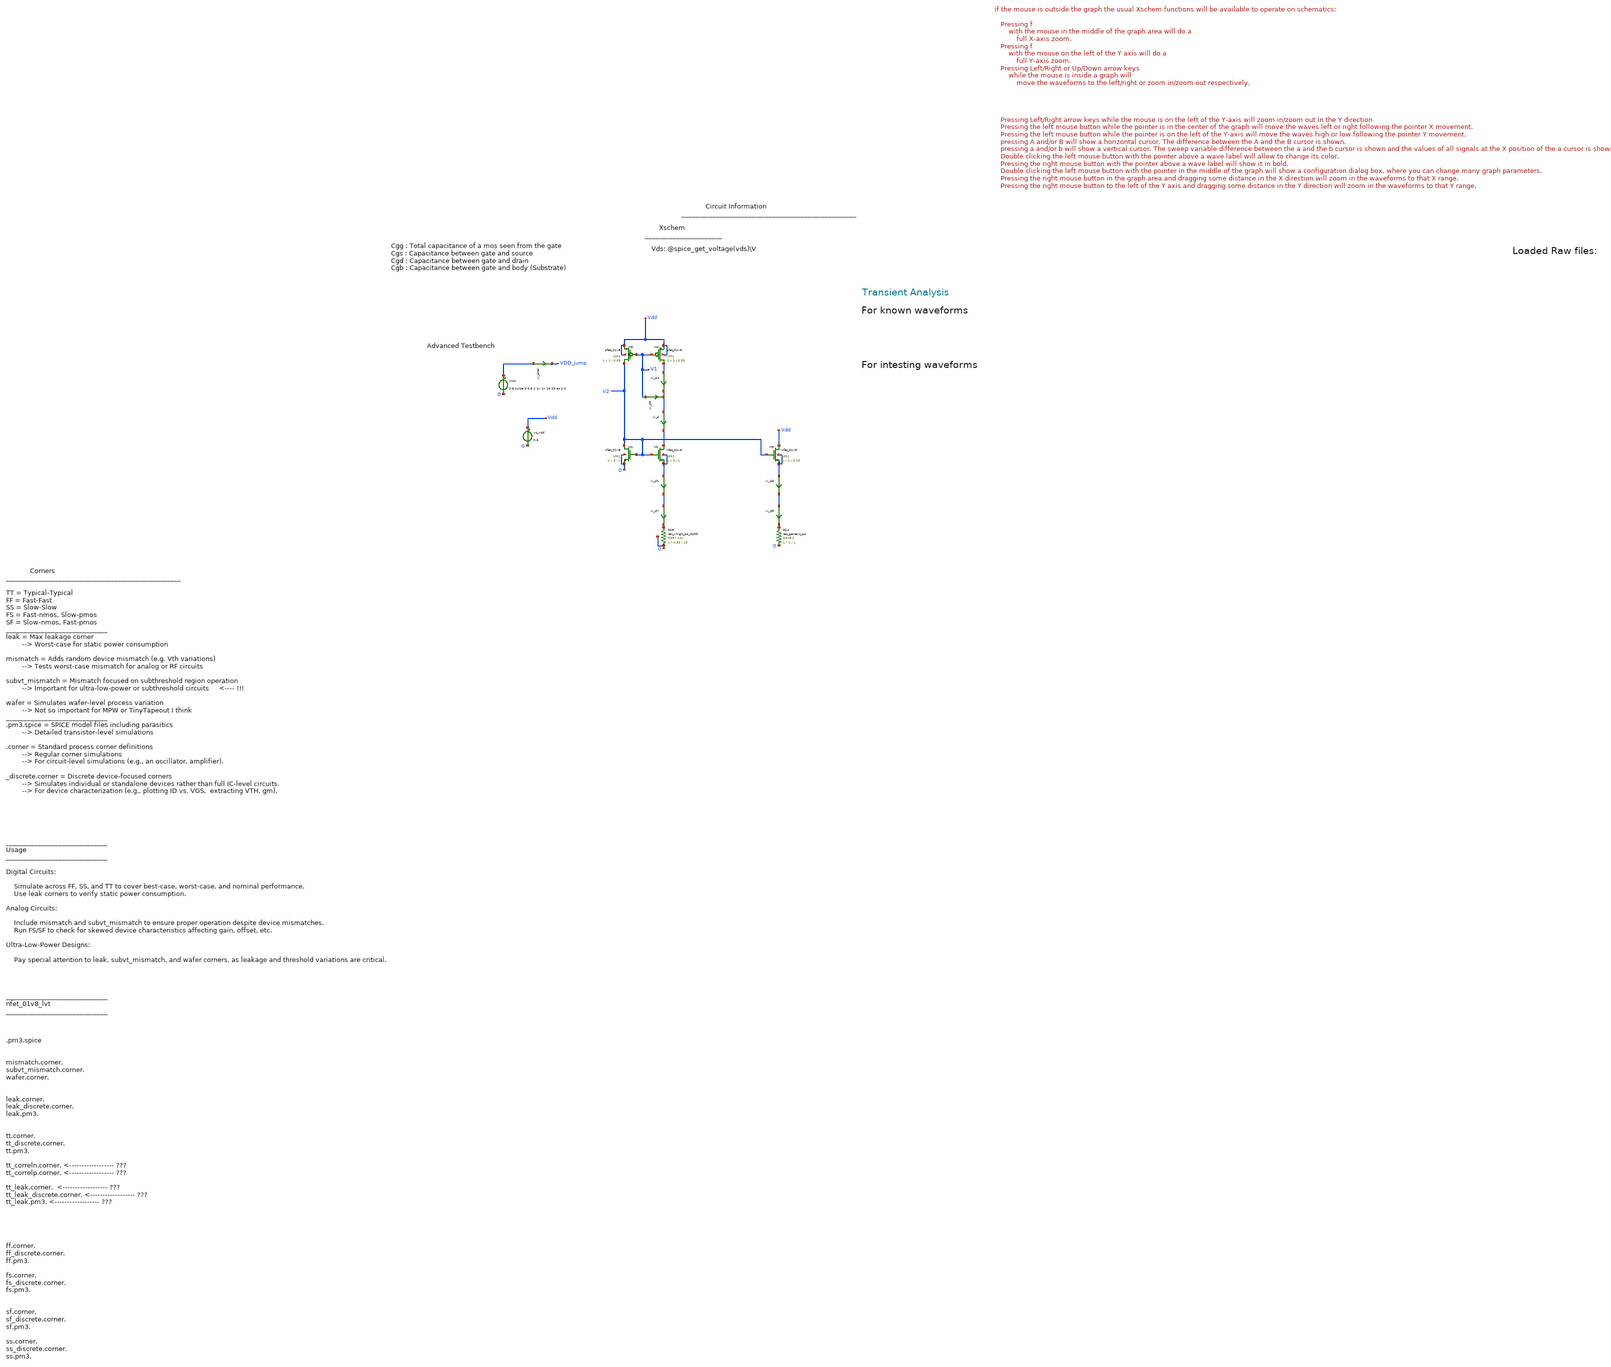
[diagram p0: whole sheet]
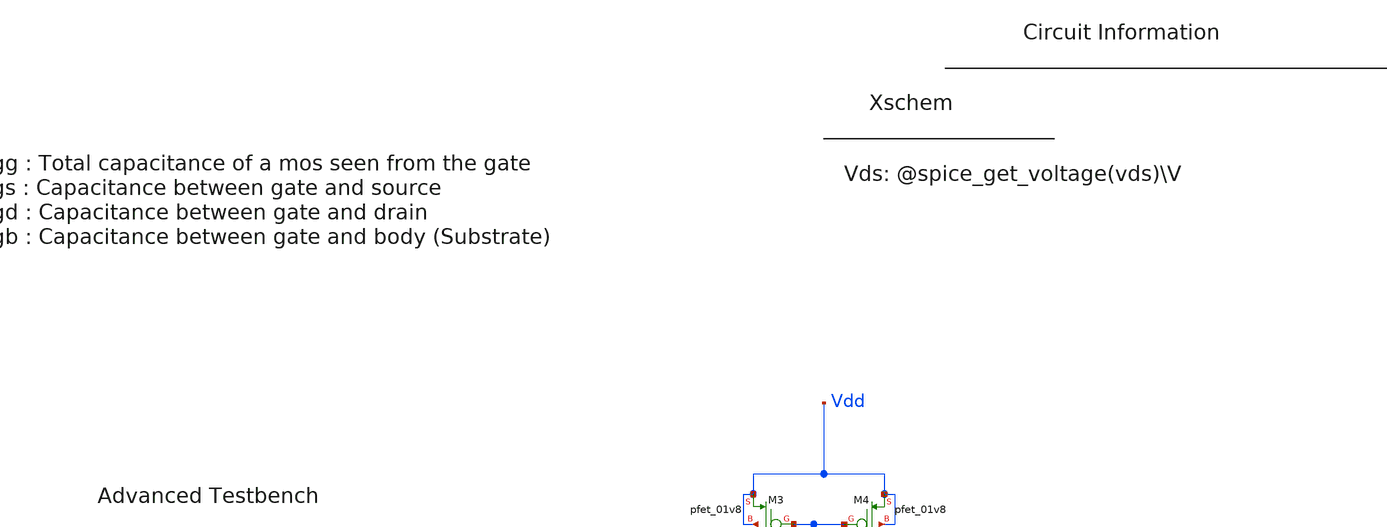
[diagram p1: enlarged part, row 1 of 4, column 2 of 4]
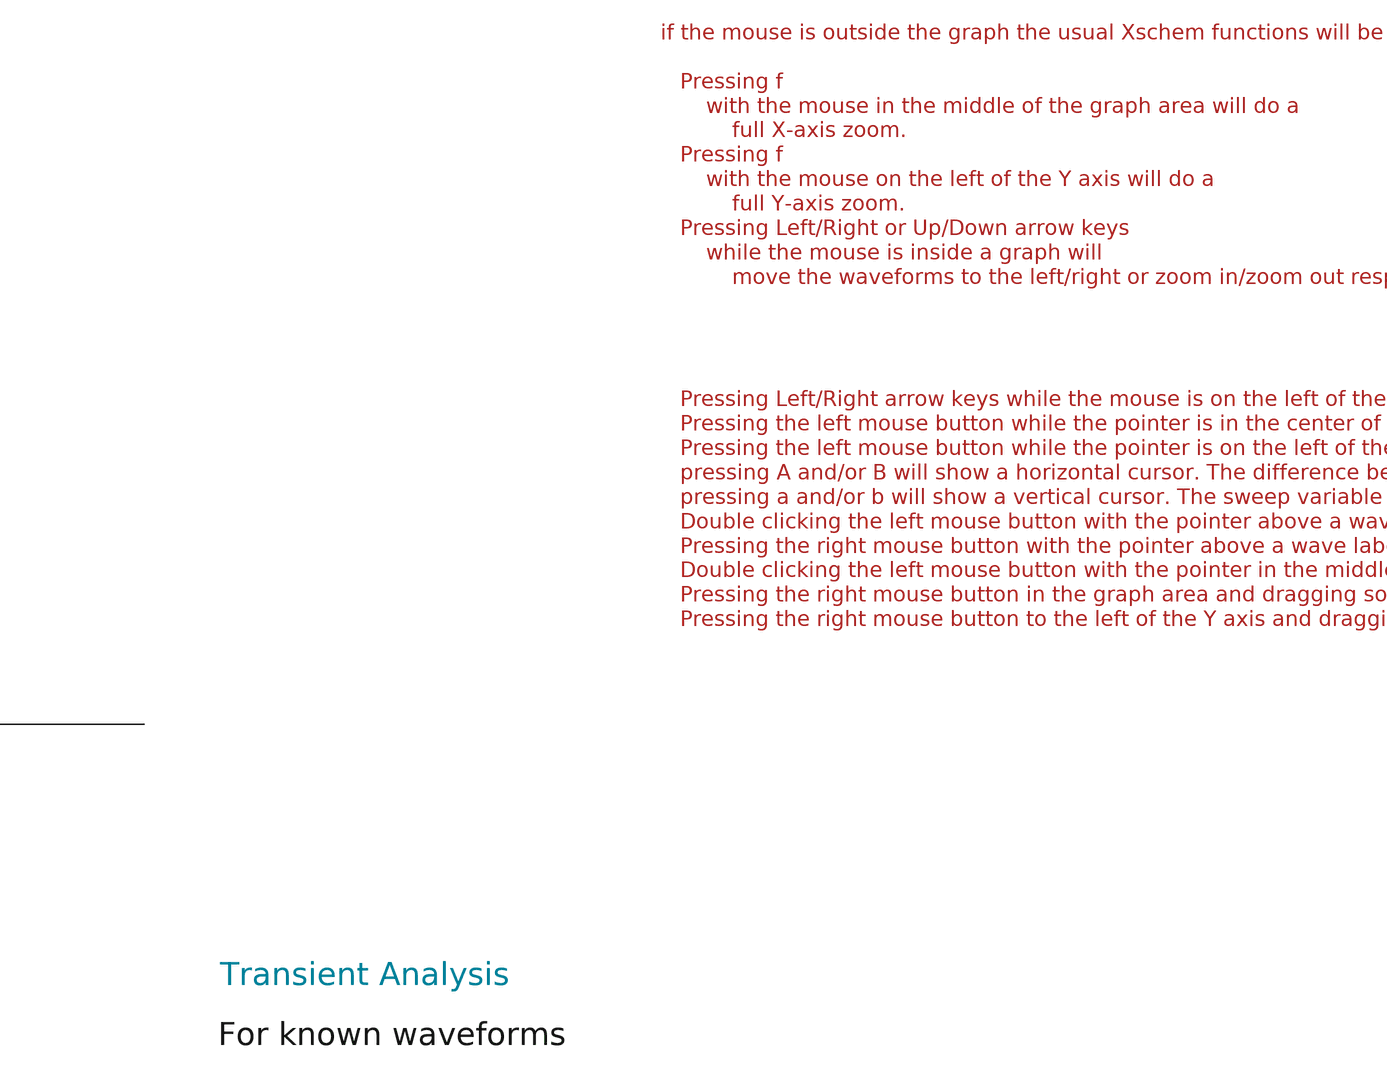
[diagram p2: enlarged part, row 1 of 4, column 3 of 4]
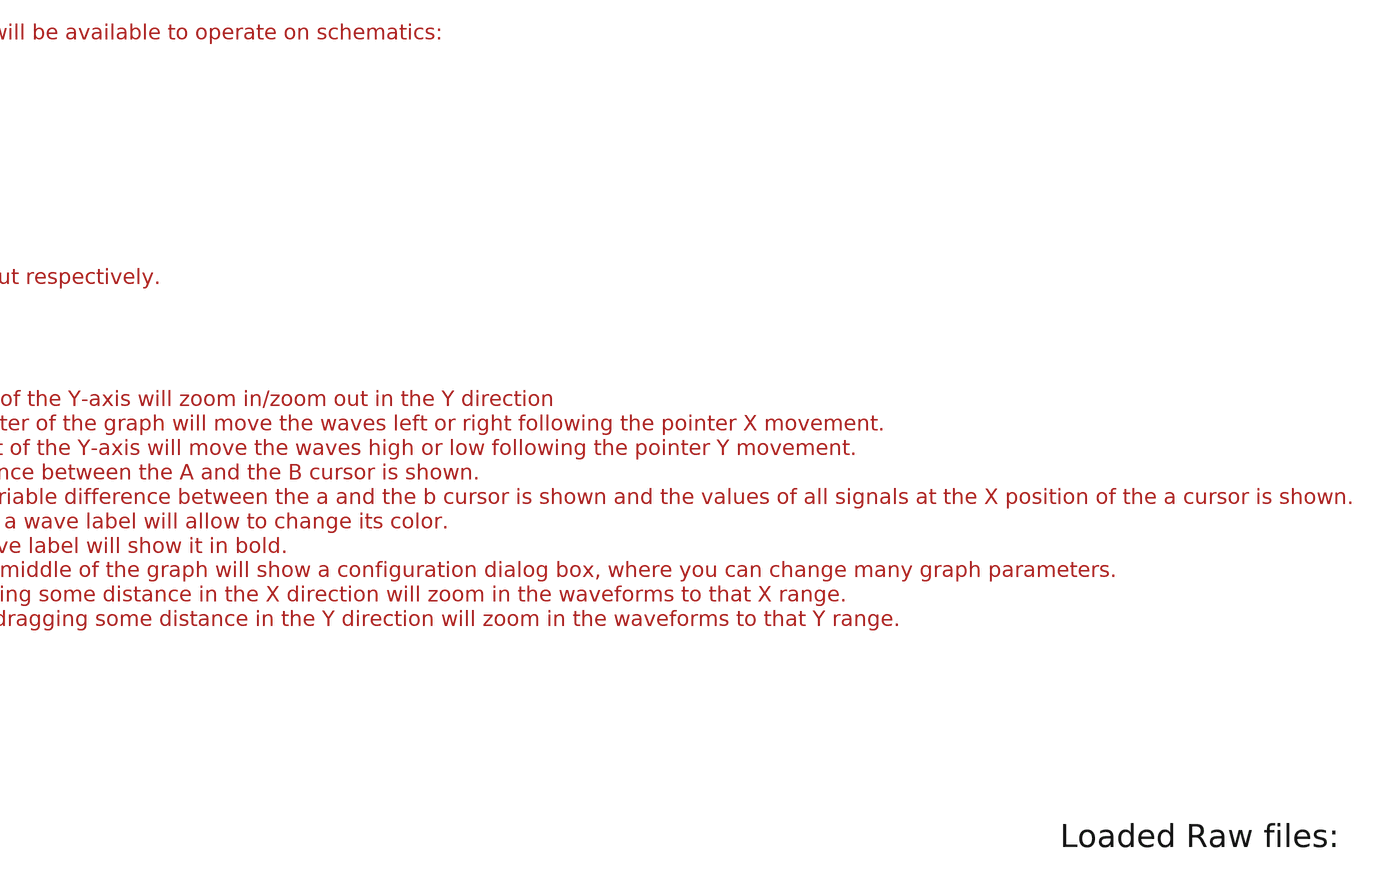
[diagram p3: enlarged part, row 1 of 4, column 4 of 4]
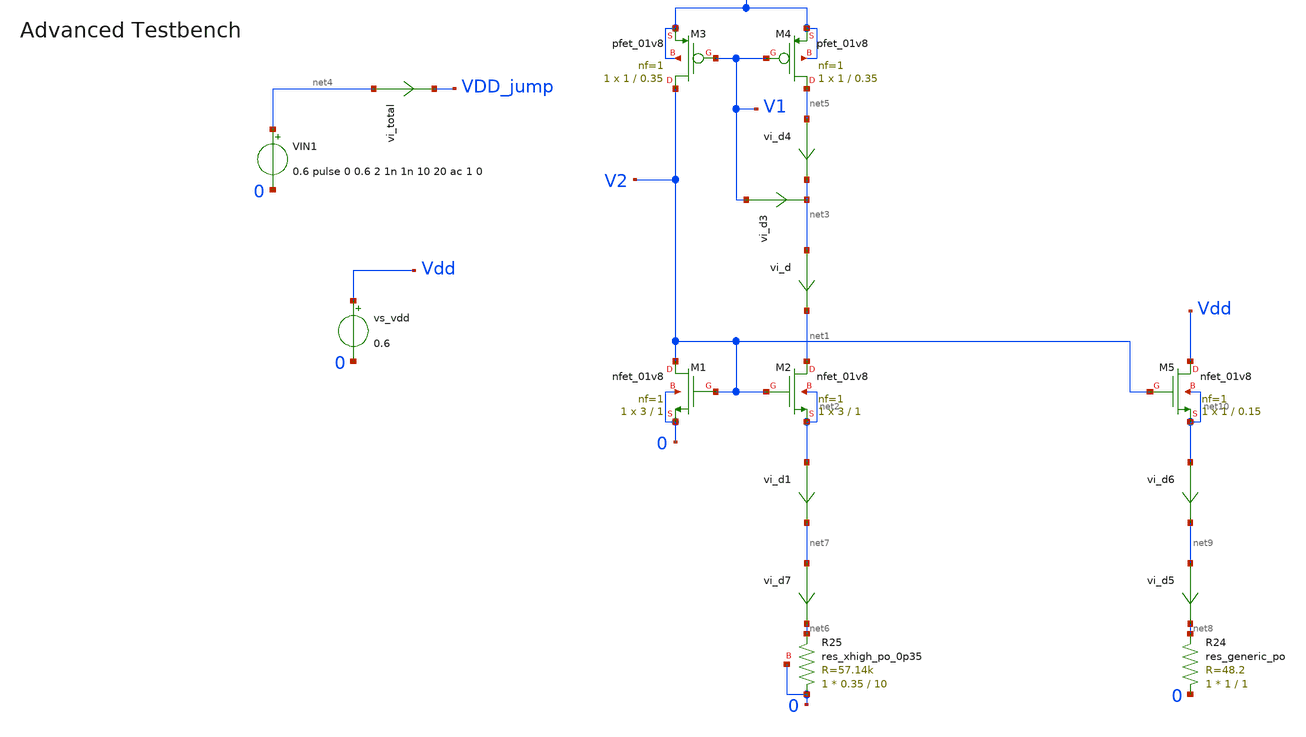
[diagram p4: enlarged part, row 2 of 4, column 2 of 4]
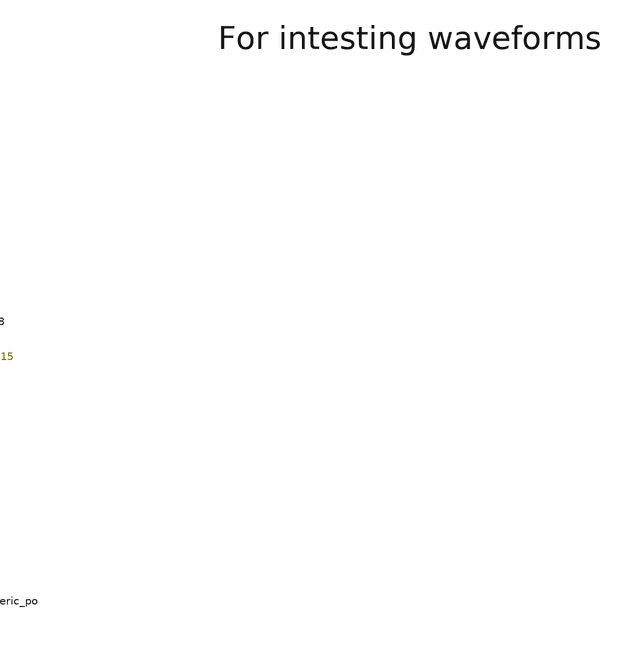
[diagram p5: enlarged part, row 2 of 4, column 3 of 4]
** sch_path: tt10-hdl/tt_um_test_commit/xschem/T2/biasGen/Z_old/weakInv_currSrc_tb.sch
* Copyright (C) 1998-2024 Stefan Frederik Schippers
* This program is free software; you can redistribute it and/or modify
* it under the terms of the GNU General Public License as published by
* the Free Software Foundation; either version 2 of the License, or
* (at your option) any later version.
* This program is distributed in the hope that it will be useful,
* but WITHOUT ANY WARRANTY; without even the implied warranty of
* MERCHANTABILITY or FITNESS FOR A PARTICULAR PURPOSE.  See the
* GNU General Public License for more details.
* You should have received a copy of the GNU General Public License
* along with this program; if not, write to the Free Software
**.subckt weakInv_currSrc_tb
vi_d net3 net1 0
.save i(vi_d)
VIN1 net4 0 0.6 pulse 0 0.6 2 1n 1n 10 20 ac 1 0
vi_d3 V1 net3 0
.save i(vi_d3)
vi_d4 net5 net3 0
.save i(vi_d4)
vi_d7 net7 net6 0
.save i(vi_d7)
vi_d1 net2 net7 0
.save i(vi_d1)
vi_d5 net9 net8 0
.save i(vi_d5)
vi_d6 net10 net9 0
.save i(vi_d6)
vi_total net4 VDD_jump 0
.save i(vi_total)
XM3 V2 V1 Vdd Vdd sky130_fd_pr__pfet_01v8 L=0.35 W=1 nf=1 ad='int((nf+1)/2) * W/nf * 0.29' as='int((nf+2)/2) * W/nf * 0.29'
+ pd='2*int((nf+1)/2) * (W/nf + 0.29)' ps='2*int((nf+2)/2) * (W/nf + 0.29)' nrd='0.29 / W' nrs='0.29 / W'
+ sa=0 sb=0 sd=0 mult=1 m=1
XM4 net5 V1 Vdd Vdd sky130_fd_pr__pfet_01v8 L=0.35 W=1 nf=1 ad='int((nf+1)/2) * W/nf * 0.29' as='int((nf+2)/2) * W/nf * 0.29'
+ pd='2*int((nf+1)/2) * (W/nf + 0.29)' ps='2*int((nf+2)/2) * (W/nf + 0.29)' nrd='0.29 / W' nrs='0.29 / W'
+ sa=0 sb=0 sd=0 mult=1 m=1
XM1 V2 V2 0 0 sky130_fd_pr__nfet_01v8 L=1 W=3 nf=1 ad='int((1 + 1)/2) * 3 / 1 * 0.29' as='int((1 + 2)/2) * 3 / 1 * 0.29'
+ pd='2*int((1 + 1)/2) * (3 / 1 + 0.29)' ps='2*int((1 + 2)/2) * (3 / 1 + 0.29)' nrd='0.29 / 3 ' nrs='0.29 / 3 '
+ sa=0 sb=0 sd=0 mult=1 m=1
XM2 net1 V2 net2 net2 sky130_fd_pr__nfet_01v8 L=1 W=3 nf=1 ad='int((1 + 1)/2) * 3 / 1 * 0.29' as='int((1 + 2)/2) * 3 / 1 * 0.29'
+ pd='2*int((1 + 1)/2) * (3 / 1 + 0.29)' ps='2*int((1 + 2)/2) * (3 / 1 + 0.29)' nrd='0.29 / 3 ' nrs='0.29 / 3 '
+ sa=0 sb=0 sd=0 mult=1 m=1
XM5 Vdd V2 net10 net10 sky130_fd_pr__nfet_01v8 L=0.15 W=1 nf=1 ad='int((1 + 1)/2) * 1 / 1 * 0.29' as='int((1 + 2)/2) * 1 / 1 * 0.29'
+ pd='2*int((1 + 1)/2) * (1 / 1 + 0.29)' ps='2*int((1 + 2)/2) * (1 / 1 + 0.29)' nrd='0.29 / 1 ' nrs='0.29 / 1 '
+ sa=0 sb=0 sd=0 mult=1 m=1
XR24 0 net8 sky130_fd_pr__res_generic_po W=1 L=1 m=1
vs_vdd Vdd 0 0.6
XR25 0 net6 0 sky130_fd_pr__res_xhigh_po_0p35 L=10 mult=1 m=1
**** begin user architecture code



.temp 30

*.option gmin=5n
*.option scale=1e-6
.option wnflag=1
.option savecurrents

.save all
.control
  save all alli

  save @m.xm1.msky130_fd_pr__nfet_01v8[gm]
  save @m.xm1.msky130_fd_pr__nfet_01v8[id]
  save @m.xm1.msky130_fd_pr__nfet_01v8[vgs]

  save @m.xm1.msky130_fd_pr__nfet_01v8[cgg]
  save @m.xm1.msky130_fd_pr__nfet_01v8[cgs]
  save @m.xm1.msky130_fd_pr__nfet_01v8[cgdo]
  save @m.xm1.msky130_fd_pr__nfet_01v8[cgb]

  save @m.xm1.msky130_fd_pr__nfet_01v8[vds]
  save @m.xm1.msky130_fd_pr__nfet_01v8[vdsat]
  save @m.xm1.msky130_fd_pr__nfet_01v8[vth]


  save @m.xm1.msky130_fd_pr__nfet_01v8[leff]
  save @m.xm1.msky130_fd_pr__nfet_01v8[weff]
  save @m.xm1.msky130_fd_pr__nfet_01v8[gds]
  save @m.xm1.msky130_fd_pr__nfet_01v8[l]
  save @m.xm1.msky130_fd_pr__nfet_01v8[w]
  save @m.xm1.msky130_fd_pr__nfet_01v8[gm]
  save @m.xm1.msky130_fd_pr__nfet_01v8[gm]
  save @m.xm1.msky130_fd_pr__nfet_01v8[gm]
  save @m.xm1.msky130_fd_pr__nfet_01v8[gm]
  save @m.xm1.msky130_fd_pr__nfet_01v8[gm]



  *dc v_dev_vds 0 1.8 0.005 v_dev_vgs 0 1.8 0.2
  *write nmos_tb.raw




  tran 1m 5000m
  write nmos_tb_tran.raw

  op
  set appendwrite
  write nmos_tb_tran.raw






  *quit 0




.endc





** opencircuitdesign pdks install
.lib $::SKYWATER_MODELS/sky130.lib.spice tt
.include $::SKYWATER_STDCELLS/sky130_fd_sc_hd.spice


**** end user architecture code
**.ends
.end
